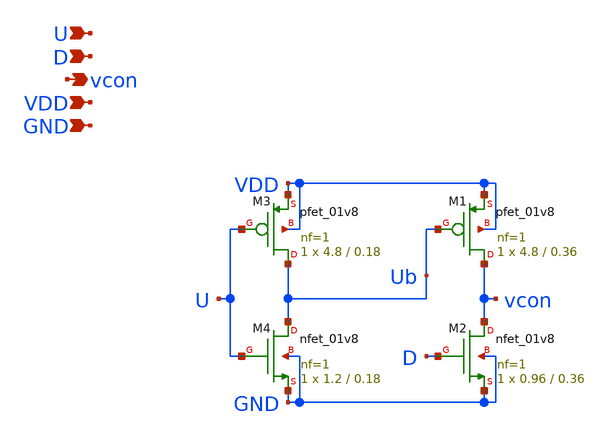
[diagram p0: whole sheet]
** sch_path: xschem/charge-pump.sch
**.subckt charge-pump U D vcon VDD GND
*.ipin U
*.ipin D
*.opin vcon
*.ipin VDD
*.ipin GND
XM1 vcon Ub VDD VDD sky130_fd_pr__pfet_01v8 L=0.36 W=4.8 nf=1 ad='int((nf+1)/2) * W/nf * 0.29' as='int((nf+2)/2) * W/nf * 0.29'
+ pd='2*int((nf+1)/2) * (W/nf + 0.29)' ps='2*int((nf+2)/2) * (W/nf + 0.29)' nrd='0.29 / W' nrs='0.29 / W'
+ sa=0 sb=0 sd=0 mult=1 m=1
XM2 vcon D GND GND sky130_fd_pr__nfet_01v8 L=0.36 W=0.96 nf=1 ad='int((nf+1)/2) * W/nf * 0.29' as='int((nf+2)/2) * W/nf * 0.29'
+ pd='2*int((nf+1)/2) * (W/nf + 0.29)' ps='2*int((nf+2)/2) * (W/nf + 0.29)' nrd='0.29 / W' nrs='0.29 / W'
+ sa=0 sb=0 sd=0 mult=1 m=1
XM3 Ub U VDD VDD sky130_fd_pr__pfet_01v8 L=0.18 W=4.8 nf=1 ad='int((nf+1)/2) * W/nf * 0.29' as='int((nf+2)/2) * W/nf * 0.29'
+ pd='2*int((nf+1)/2) * (W/nf + 0.29)' ps='2*int((nf+2)/2) * (W/nf + 0.29)' nrd='0.29 / W' nrs='0.29 / W'
+ sa=0 sb=0 sd=0 mult=1 m=1
XM4 Ub U GND GND sky130_fd_pr__nfet_01v8 L=0.18 W=1.2 nf=1 ad='int((nf+1)/2) * W/nf * 0.29' as='int((nf+2)/2) * W/nf * 0.29'
+ pd='2*int((nf+1)/2) * (W/nf + 0.29)' ps='2*int((nf+2)/2) * (W/nf + 0.29)' nrd='0.29 / W' nrs='0.29 / W'
+ sa=0 sb=0 sd=0 mult=1 m=1
**.ends
.end
